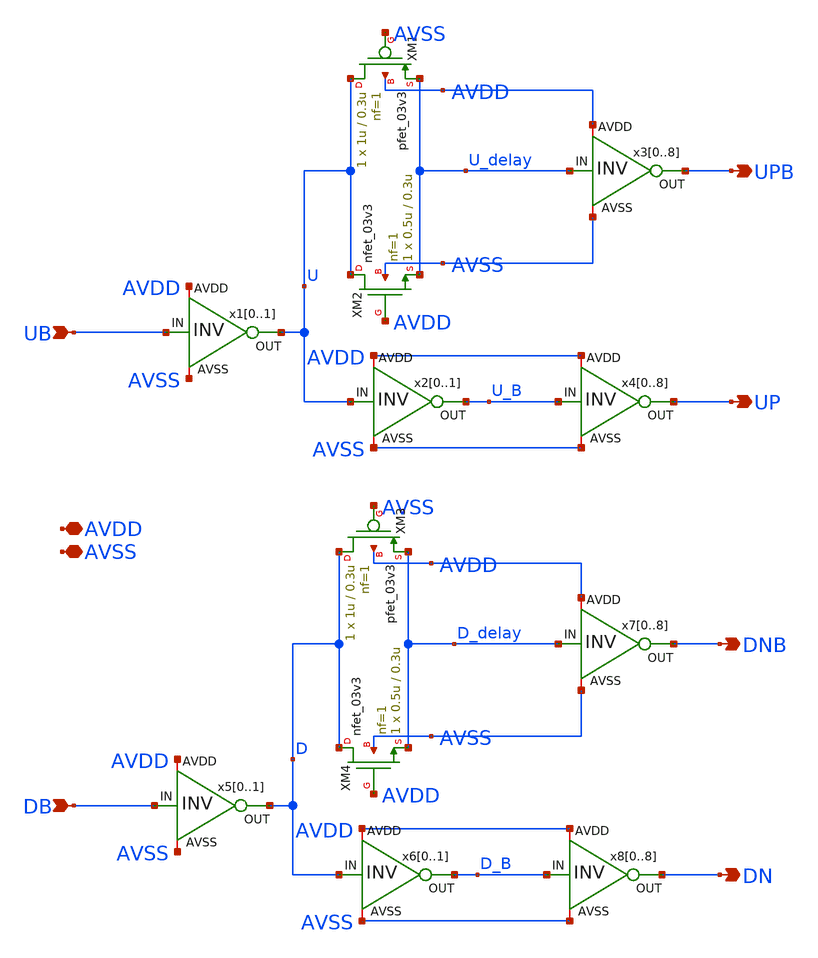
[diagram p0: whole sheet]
** sch_path: designs/libs/core_analog/pfd_s2d/pfd_s2d.sch
**.subckt pfd_s2d UB DB AVDD AVSS UP UPB DN DNB
*.ipin UB
*.ipin DB
*.iopin AVDD
*.iopin AVSS
*.opin UP
*.opin UPB
*.opin DN
*.opin DNB
XM1 U AVSS U_delay AVDD pfet_03v3 L=0.3u W=1u nf=1 ad='int((nf+1)/2) * W/nf * 0.18u' as='int((nf+2)/2) * W/nf * 0.18u'
+ pd='2*int((nf+1)/2) * (W/nf + 0.18u)' ps='2*int((nf+2)/2) * (W/nf + 0.18u)' nrd='0.18u / W' nrs='0.18u / W'
+ sa=0 sb=0 sd=0 m=1
XM2 U AVDD U_delay AVSS nfet_03v3 L=0.3u W=0.5u nf=1 ad='int((nf+1)/2) * W/nf * 0.18u' as='int((nf+2)/2) * W/nf * 0.18u'
+ pd='2*int((nf+1)/2) * (W/nf + 0.18u)' ps='2*int((nf+2)/2) * (W/nf + 0.18u)' nrd='0.18u / W' nrs='0.18u / W'
+ sa=0 sb=0 sd=0 m=1
x10 AVDD UB U AVSS inv
x11 AVDD UB U AVSS inv
x20 AVDD U U_B AVSS inv
x21 AVDD U U_B AVSS inv
x30 AVDD U_delay UPB AVSS inv
x31 AVDD U_delay UPB AVSS inv
x32 AVDD U_delay UPB AVSS inv
x33 AVDD U_delay UPB AVSS inv
x34 AVDD U_delay UPB AVSS inv
x35 AVDD U_delay UPB AVSS inv
x36 AVDD U_delay UPB AVSS inv
x37 AVDD U_delay UPB AVSS inv
x38 AVDD U_delay UPB AVSS inv
x40 AVDD U_B UP AVSS inv
x41 AVDD U_B UP AVSS inv
x42 AVDD U_B UP AVSS inv
x43 AVDD U_B UP AVSS inv
x44 AVDD U_B UP AVSS inv
x45 AVDD U_B UP AVSS inv
x46 AVDD U_B UP AVSS inv
x47 AVDD U_B UP AVSS inv
x48 AVDD U_B UP AVSS inv
x50 AVDD DB D AVSS inv
x51 AVDD DB D AVSS inv
x60 AVDD D D_B AVSS inv
x61 AVDD D D_B AVSS inv
x70 AVDD D_delay DNB AVSS inv
x71 AVDD D_delay DNB AVSS inv
x72 AVDD D_delay DNB AVSS inv
x73 AVDD D_delay DNB AVSS inv
x74 AVDD D_delay DNB AVSS inv
x75 AVDD D_delay DNB AVSS inv
x76 AVDD D_delay DNB AVSS inv
x77 AVDD D_delay DNB AVSS inv
x78 AVDD D_delay DNB AVSS inv
x80 AVDD D_B DN AVSS inv
x81 AVDD D_B DN AVSS inv
x82 AVDD D_B DN AVSS inv
x83 AVDD D_B DN AVSS inv
x84 AVDD D_B DN AVSS inv
x85 AVDD D_B DN AVSS inv
x86 AVDD D_B DN AVSS inv
x87 AVDD D_B DN AVSS inv
x88 AVDD D_B DN AVSS inv
XM3 D AVSS D_delay AVDD pfet_03v3 L=0.3u W=1u nf=1 ad='int((nf+1)/2) * W/nf * 0.18u' as='int((nf+2)/2) * W/nf * 0.18u'
+ pd='2*int((nf+1)/2) * (W/nf + 0.18u)' ps='2*int((nf+2)/2) * (W/nf + 0.18u)' nrd='0.18u / W' nrs='0.18u / W'
+ sa=0 sb=0 sd=0 m=1
XM4 D AVDD D_delay AVSS nfet_03v3 L=0.3u W=0.5u nf=1 ad='int((nf+1)/2) * W/nf * 0.18u' as='int((nf+2)/2) * W/nf * 0.18u'
+ pd='2*int((nf+1)/2) * (W/nf + 0.18u)' ps='2*int((nf+2)/2) * (W/nf + 0.18u)' nrd='0.18u / W' nrs='0.18u / W'
+ sa=0 sb=0 sd=0 m=1
**.ends

* expanding   symbol:  libs/core_analog/inv/inv.sym # of pins=4
** sym_path: designs/libs/core_analog/inv/inv.sym
** sch_path: designs/libs/core_analog/inv/inv.sch
.subckt inv AVDD IN OUT AVSS
*.ipin IN
*.iopin AVDD
*.iopin AVSS
*.opin OUT
XM1 OUT IN AVDD AVDD pfet_03v3 L=0.28u W=0.9u nf=1 ad='int((nf+1)/2) * W/nf * 0.18u' as='int((nf+2)/2) * W/nf * 0.18u'
+ pd='2*int((nf+1)/2) * (W/nf + 0.18u)' ps='2*int((nf+2)/2) * (W/nf + 0.18u)' nrd='0.18u / W' nrs='0.18u / W'
+ sa=0 sb=0 sd=0 m=1
XM2 OUT IN AVSS AVSS nfet_03v3 L=0.28u W=0.3u nf=1 ad='int((nf+1)/2) * W/nf * 0.18u' as='int((nf+2)/2) * W/nf * 0.18u'
+ pd='2*int((nf+1)/2) * (W/nf + 0.18u)' ps='2*int((nf+2)/2) * (W/nf + 0.18u)' nrd='0.18u / W' nrs='0.18u / W'
+ sa=0 sb=0 sd=0 m=1
.ends

.end
